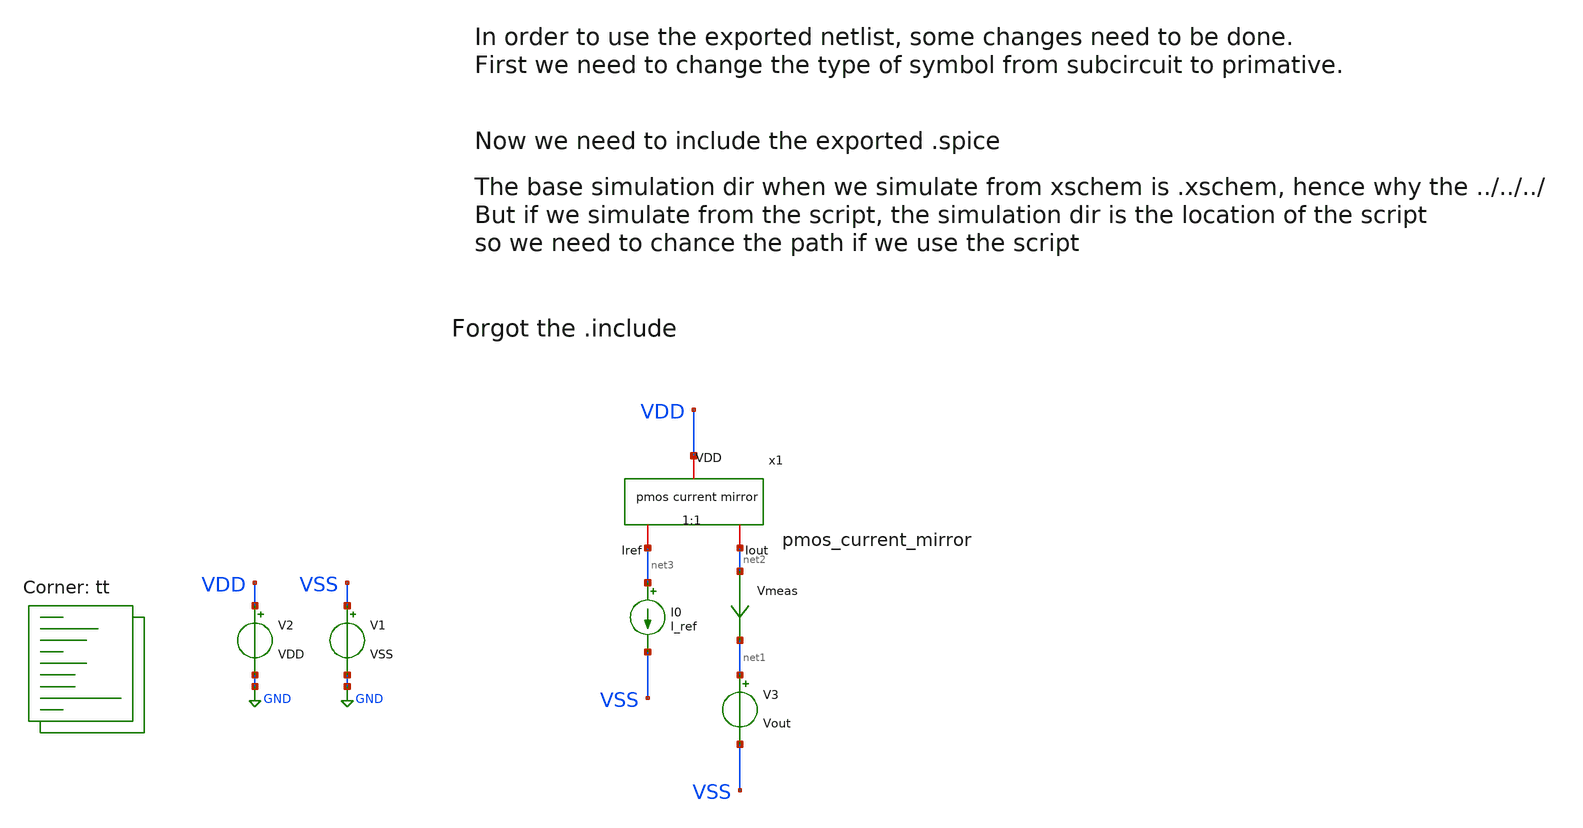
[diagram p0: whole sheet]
** sch_path: Learning/Current_mirrors/Design_pmos_current_mirror_sky130_5v/simulation/current_mirror_tb_.sch
**.subckt current_mirror_tb_
V1 VSS GND VSS
I0 net3 VSS I_ref
V2 VDD GND VDD
V3 net1 VSS Vout
Vmeas net2 net1 0
.save i(vmeas)
x1 VDD net3 net2 pmos_current_mirror
**** begin user architecture code
.lib $::SKYWATER_MODELS/sky130.lib.spice tt


.param VDD = 5
.param VSS = 0
.param I_ref = 5u
.param Vout = 0


*.include ../../../foss/designs/OSAD/Learning/Current_mirrors/Design_pmos_current_mirror_sky130_5v/pmos_current_mirror_layout/pmos_current_mirror.spice
.include ../pmos_current_mirror_layout/pmos_current_mirror.spice

.control
op
dc V3 0 5 0.001
plot i(Vmeas)
wrdata current_tb.csv i(Vmeas)
.endc


**** end user architecture code
**.ends
.GLOBAL GND
.end
